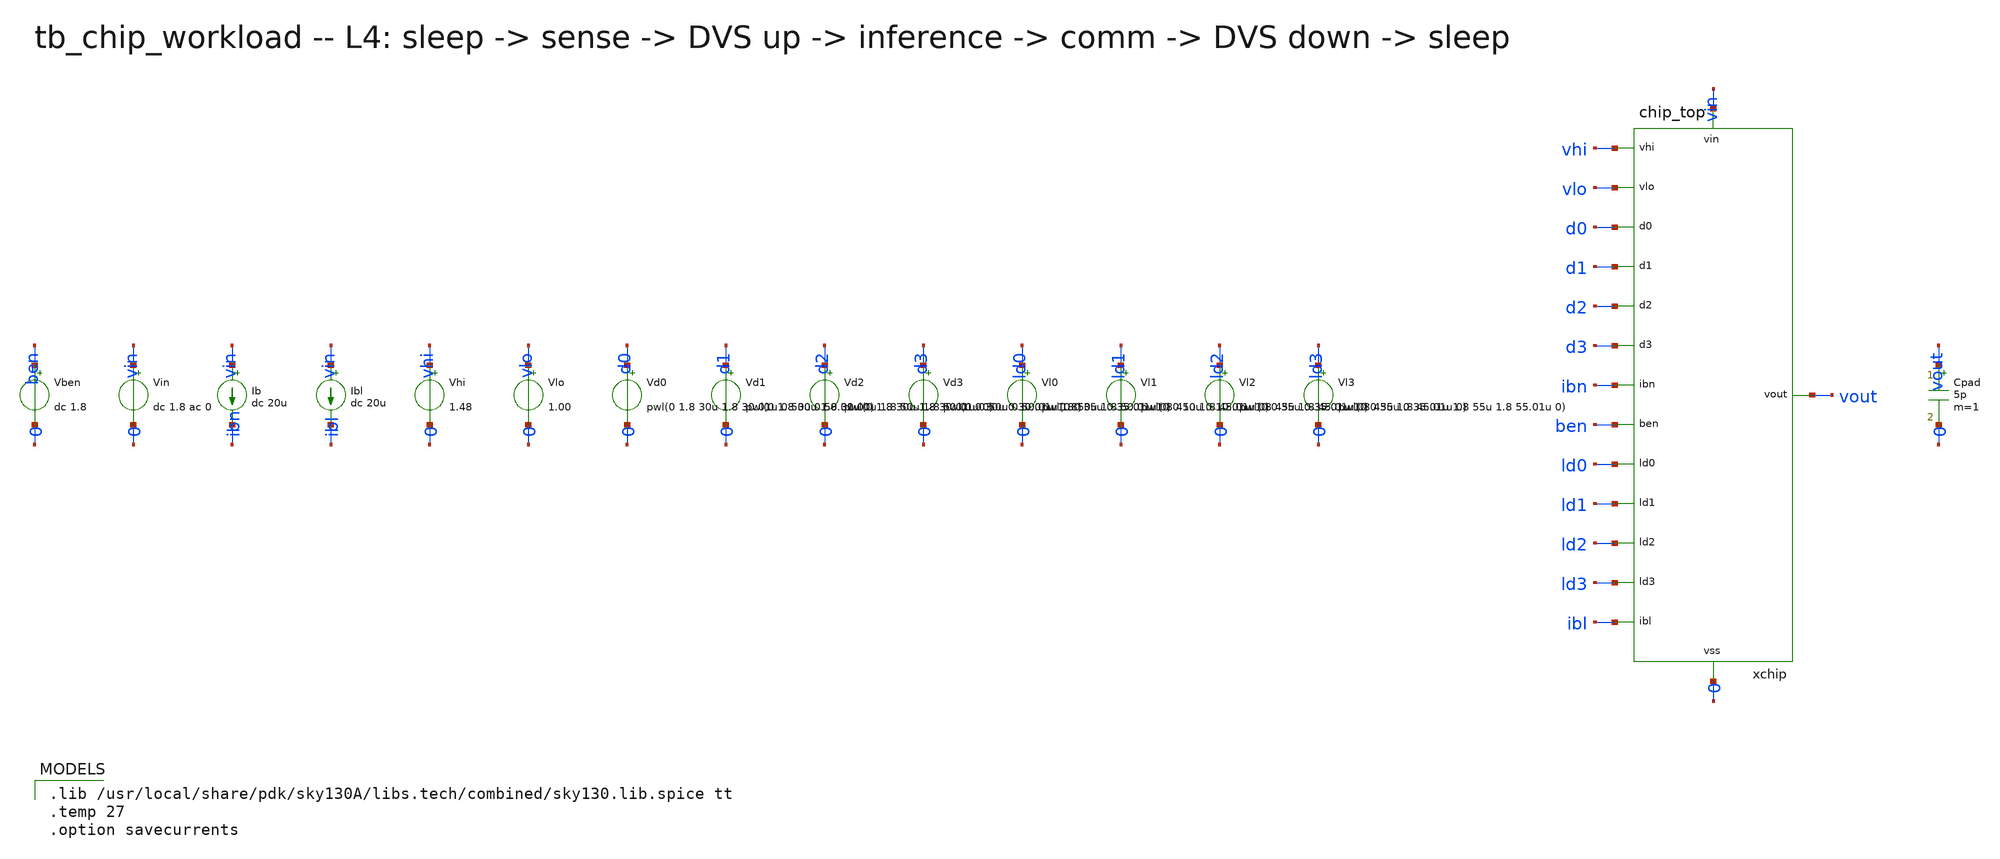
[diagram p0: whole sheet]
** sch_path: xschem/onetops_tb/tb_chip_workload.sch
**.subckt tb_chip_workload
Vin vin 0 dc 1.8 ac 0
Ib vin ibn dc 20u
Vben ben 0 dc 1.8
Ibl vin ibl dc 20u
Vhi vhi 0 1.48
Vlo vlo 0 1.00
Vd0 d0 0 pwl(0 1.8 30u 1.8 30.01u 0 50u 0 50.01u 0)
Vd1 d1 0 pwl(0 1.8 30u 1.8 30.01u 1.8 50u 1.8 50.01u 0)
Vd2 d2 0 pwl(0 1.8 30u 1.8 30.01u 0 50u 0 50.01u 1.8)
Vd3 d3 0 pwl(0 0 30u 0 30.01u 1.8 50u 1.8 50.01u 0)
Vl0 ld0 0 pwl(0 0 35u 0 35.01u 1.8 45u 1.8 45.01u 0)
Vl1 ld1 0 pwl(0 0 10u 0 10.01u 1.8 45u 1.8 45.01u 0)
Vl2 ld2 0 pwl(0 0 35u 0 35.01u 1.8 45u 1.8 45.01u 0)
Vl3 ld3 0 pwl(0 0 35u 0 35.01u 1.8 55u 1.8 55.01u 0)
xchip vhi vlo d0 d1 d2 d3 ibn ben ld0 ld1 ld2 ld3 ibl vout vin 0 chip_top
Cpad vout 0 5p m=1
**** begin user architecture code

.lib /usr/local/share/pdk/sky130A/libs.tech/combined/sky130.lib.spice tt
.temp 27
.option savecurrents


.control
foreach ben 1.8 0
alter @vben[dc]=$ben
echo WORKLOAD BEN=$ben
tran 5n 70u 0 1n
meas tran v_sleep find v(vout) at=9.5u
meas tran v_sense find v(vout) at=29u
meas tran v_pre find v(vout) at=34.9u
meas tran vmin_inf min v(vout) from=35u to=40u
meas tran v_inf find v(vout) at=44.9u
meas tran vmax_comm max v(vout) from=45u to=48u
meas tran v_comm find v(vout) at=49.9u
meas tran v_low find v(vout) at=54.9u
meas tran vmax_sleep max v(vout) from=55u to=58u
let under_inf_mV = (v_pre - vmin_inf)*1000
let over_comm_mV = (vmax_comm - v_inf)*1000
let over_sleep_mV = (vmax_sleep - v_low)*1000
print under_inf_mV over_comm_mV over_sleep_mV
meas tran iin_avg avg i(vin) from=0 to=70u
let iavg_mA = -iin_avg*1000
print iavg_mA
if $?batchmode
else
  plot v(vout) title workload-ben=$ben
end
end
.endc

**** end user architecture code
**.ends
.end
